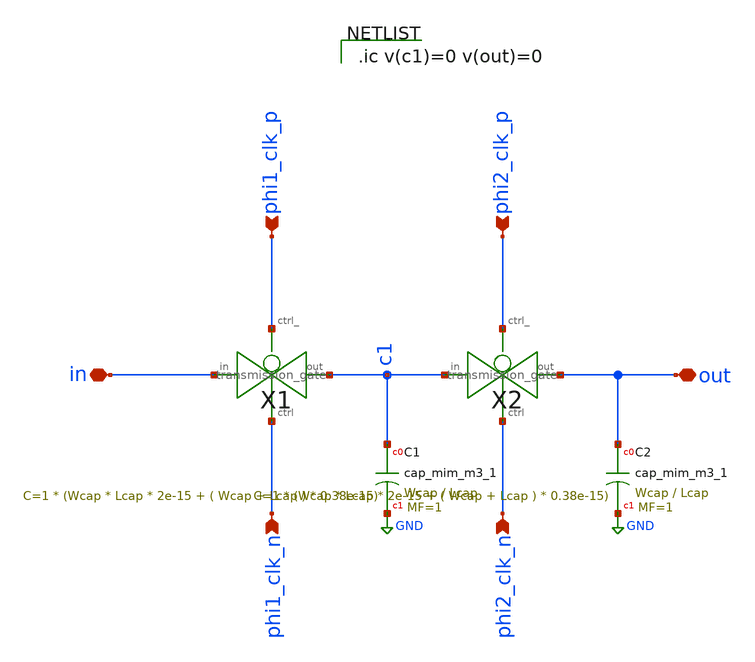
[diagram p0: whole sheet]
** sch_path: xschem/Switched_Caps/2switchcaps.sch
**.subckt 2switchcaps out in phi1_clk_n phi1_clk_p phi2_clk_p phi2_clk_n
*.iopin out
*.iopin in
*.ipin phi1_clk_n
*.ipin phi1_clk_p
*.ipin phi2_clk_p
*.ipin phi2_clk_n
XC1 c1 GND sky130_fd_pr__cap_mim_m3_1 W=Wcap L=Lcap MF=1 m=1
X1 in c1 phi1_clk_p phi1_clk_n transmission_gate
X2 c1 out phi2_clk_p phi2_clk_n transmission_gate
XC2 out GND sky130_fd_pr__cap_mim_m3_1 W=Wcap L=Lcap MF=1 m=1
**** begin user architecture code

.ic v(c1)=0 v(out)=0

**** end user architecture code
**.ends

* expanding   symbol:  transmission_gate/transmission_gate.sym # of pins=4
** sym_path: xschem/transmission_gate/transmission_gate.sym
** sch_path: xschem/transmission_gate/transmission_gate.sch
.subckt transmission_gate in out ctrl_ ctrl
*.iopin in
*.iopin out
*.ipin ctrl_
*.ipin ctrl
XM3 in ctrl out GND sky130_fd_pr__nfet_01v8 L=0.18 W=1 nf=1 ad='int((nf+1)/2) * W/nf * 0.29' as='int((nf+2)/2) * W/nf * 0.29'
+ pd='2*int((nf+1)/2) * (W/nf + 0.29)' ps='2*int((nf+2)/2) * (W/nf + 0.29)' nrd='0.29 / W' nrs='0.29 / W'
+ sa=0 sb=0 sd=0 mult=1 m=1
XM4 out ctrl_ in VDD sky130_fd_pr__pfet_01v8 L=0.18 W=1 nf=1 ad='int((nf+1)/2) * W/nf * 0.29' as='int((nf+2)/2) * W/nf * 0.29'
+ pd='2*int((nf+1)/2) * (W/nf + 0.29)' ps='2*int((nf+2)/2) * (W/nf + 0.29)' nrd='0.29 / W' nrs='0.29 / W'
+ sa=0 sb=0 sd=0 mult=1 m=1
.ends

.GLOBAL GND
.GLOBAL VDD
.end
